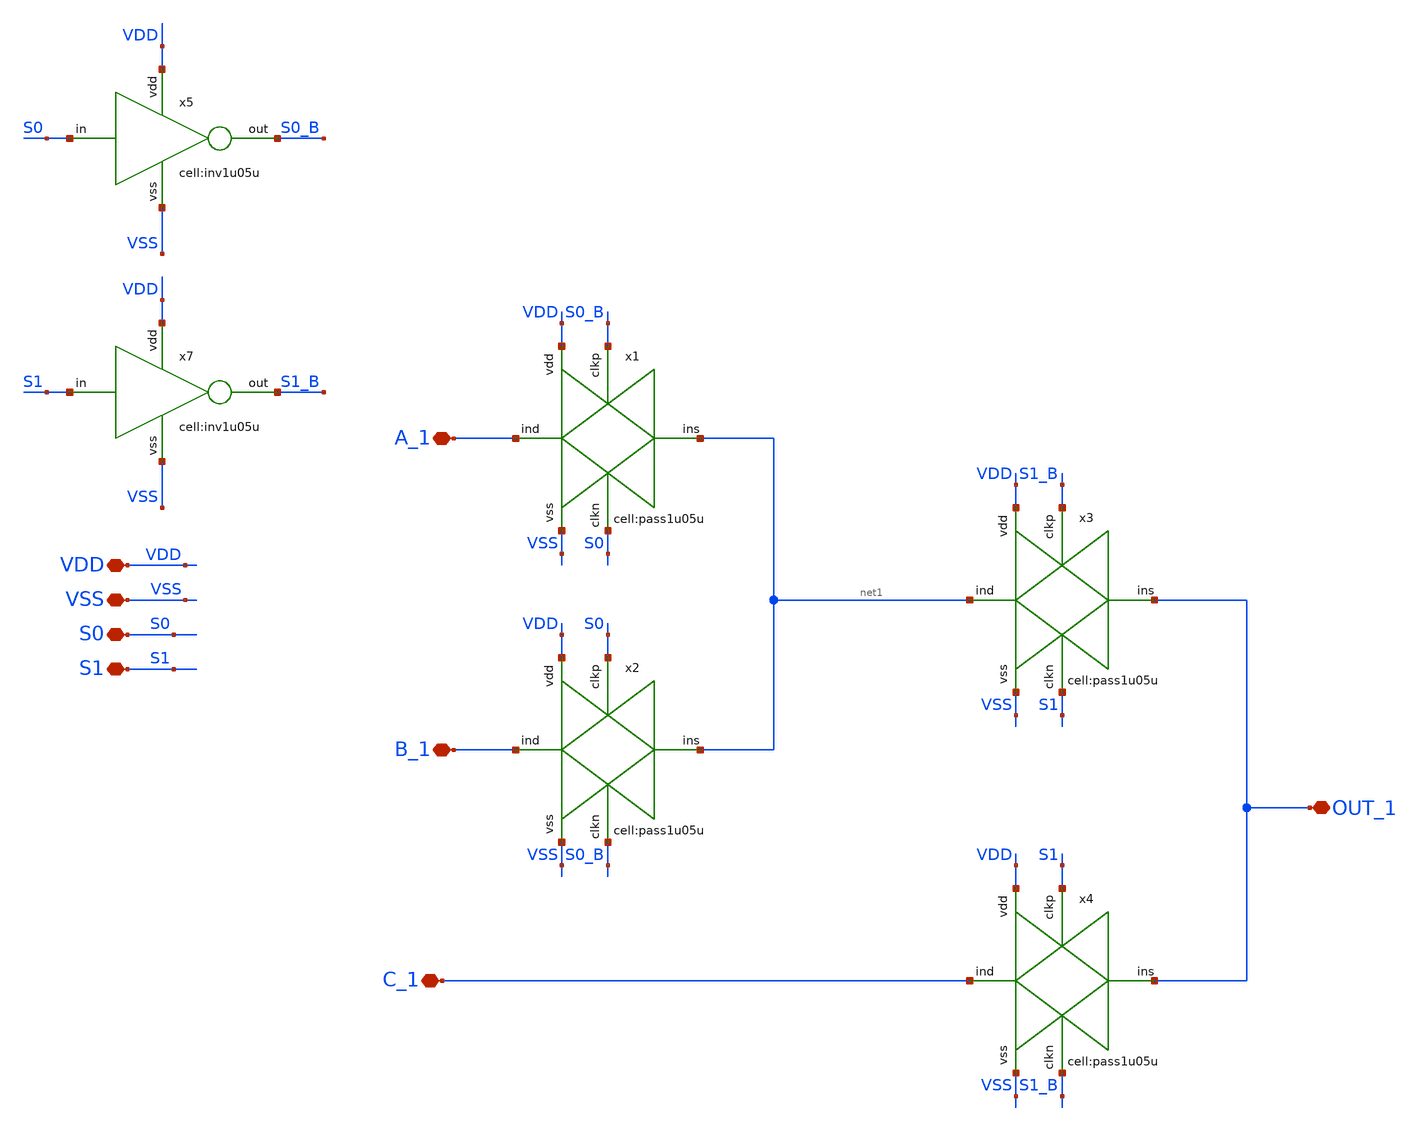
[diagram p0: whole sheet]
** sch_path: designs/libs/xp_core_analog/xp_3_1_MUX/xp_3_1_MUX.sch
**.subckt xp_3_1_MUX A_1 B_1 C_1 OUT_1 VDD VSS S0 S1
*.iopin A_1
*.iopin B_1
*.iopin C_1
*.iopin OUT_1
*.iopin VDD
*.iopin VSS
*.iopin S0
*.iopin S1
x2 B_1 VSS S0_B net1 S0 VDD pass1u05u
x1 A_1 VSS S0 net1 S0_B VDD pass1u05u
x3 net1 VSS S1 OUT_1 S1_B VDD pass1u05u
x4 C_1 VSS S1_B OUT_1 S1 VDD pass1u05u
x7 S1 VDD S1_B VSS inv1u05u
x5 S0 VDD S0_B VSS inv1u05u
**.ends
.end
